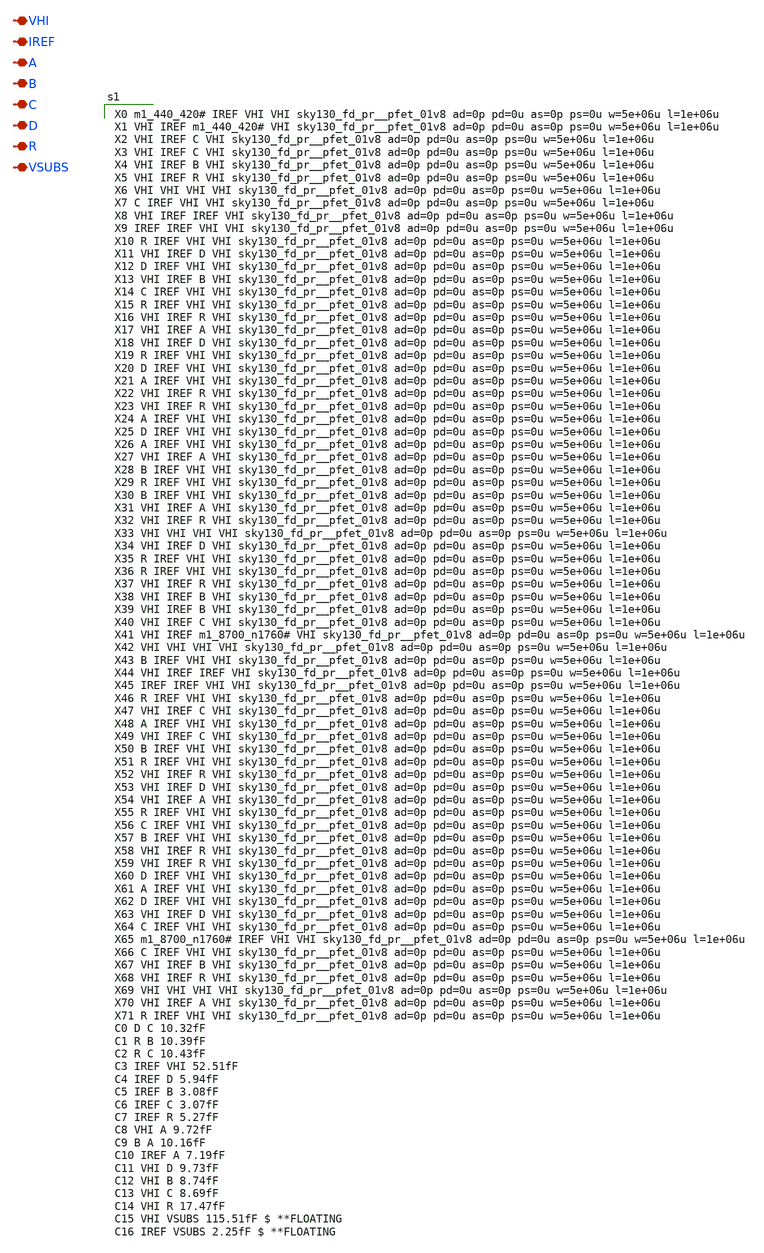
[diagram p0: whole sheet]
** sch_path: xschem/MIXER_current_dist_PEX.sch
**.subckt MIXER_current_dist_PEX IREF A B C D R VSUBS VHI
*.iopin IREF
*.iopin A
*.iopin B
*.iopin C
*.iopin D
*.iopin R
*.iopin VSUBS
*.iopin VHI
**** begin user architecture code

X0 m1_440_420# IREF VHI VHI sky130_fd_pr__pfet_01v8 ad=0p pd=0u as=0p ps=0u w=5e+06u l=1e+06u
X1 VHI IREF m1_440_420# VHI sky130_fd_pr__pfet_01v8 ad=0p pd=0u as=0p ps=0u w=5e+06u l=1e+06u
X2 VHI IREF C VHI sky130_fd_pr__pfet_01v8 ad=0p pd=0u as=0p ps=0u w=5e+06u l=1e+06u
X3 VHI IREF C VHI sky130_fd_pr__pfet_01v8 ad=0p pd=0u as=0p ps=0u w=5e+06u l=1e+06u
X4 VHI IREF B VHI sky130_fd_pr__pfet_01v8 ad=0p pd=0u as=0p ps=0u w=5e+06u l=1e+06u
X5 VHI IREF R VHI sky130_fd_pr__pfet_01v8 ad=0p pd=0u as=0p ps=0u w=5e+06u l=1e+06u
X6 VHI VHI VHI VHI sky130_fd_pr__pfet_01v8 ad=0p pd=0u as=0p ps=0u w=5e+06u l=1e+06u
X7 C IREF VHI VHI sky130_fd_pr__pfet_01v8 ad=0p pd=0u as=0p ps=0u w=5e+06u l=1e+06u
X8 VHI IREF IREF VHI sky130_fd_pr__pfet_01v8 ad=0p pd=0u as=0p ps=0u w=5e+06u l=1e+06u
X9 IREF IREF VHI VHI sky130_fd_pr__pfet_01v8 ad=0p pd=0u as=0p ps=0u w=5e+06u l=1e+06u
X10 R IREF VHI VHI sky130_fd_pr__pfet_01v8 ad=0p pd=0u as=0p ps=0u w=5e+06u l=1e+06u
X11 VHI IREF D VHI sky130_fd_pr__pfet_01v8 ad=0p pd=0u as=0p ps=0u w=5e+06u l=1e+06u
X12 D IREF VHI VHI sky130_fd_pr__pfet_01v8 ad=0p pd=0u as=0p ps=0u w=5e+06u l=1e+06u
X13 VHI IREF B VHI sky130_fd_pr__pfet_01v8 ad=0p pd=0u as=0p ps=0u w=5e+06u l=1e+06u
X14 C IREF VHI VHI sky130_fd_pr__pfet_01v8 ad=0p pd=0u as=0p ps=0u w=5e+06u l=1e+06u
X15 R IREF VHI VHI sky130_fd_pr__pfet_01v8 ad=0p pd=0u as=0p ps=0u w=5e+06u l=1e+06u
X16 VHI IREF R VHI sky130_fd_pr__pfet_01v8 ad=0p pd=0u as=0p ps=0u w=5e+06u l=1e+06u
X17 VHI IREF A VHI sky130_fd_pr__pfet_01v8 ad=0p pd=0u as=0p ps=0u w=5e+06u l=1e+06u
X18 VHI IREF D VHI sky130_fd_pr__pfet_01v8 ad=0p pd=0u as=0p ps=0u w=5e+06u l=1e+06u
X19 R IREF VHI VHI sky130_fd_pr__pfet_01v8 ad=0p pd=0u as=0p ps=0u w=5e+06u l=1e+06u
X20 D IREF VHI VHI sky130_fd_pr__pfet_01v8 ad=0p pd=0u as=0p ps=0u w=5e+06u l=1e+06u
X21 A IREF VHI VHI sky130_fd_pr__pfet_01v8 ad=0p pd=0u as=0p ps=0u w=5e+06u l=1e+06u
X22 VHI IREF R VHI sky130_fd_pr__pfet_01v8 ad=0p pd=0u as=0p ps=0u w=5e+06u l=1e+06u
X23 VHI IREF R VHI sky130_fd_pr__pfet_01v8 ad=0p pd=0u as=0p ps=0u w=5e+06u l=1e+06u
X24 A IREF VHI VHI sky130_fd_pr__pfet_01v8 ad=0p pd=0u as=0p ps=0u w=5e+06u l=1e+06u
X25 D IREF VHI VHI sky130_fd_pr__pfet_01v8 ad=0p pd=0u as=0p ps=0u w=5e+06u l=1e+06u
X26 A IREF VHI VHI sky130_fd_pr__pfet_01v8 ad=0p pd=0u as=0p ps=0u w=5e+06u l=1e+06u
X27 VHI IREF A VHI sky130_fd_pr__pfet_01v8 ad=0p pd=0u as=0p ps=0u w=5e+06u l=1e+06u
X28 B IREF VHI VHI sky130_fd_pr__pfet_01v8 ad=0p pd=0u as=0p ps=0u w=5e+06u l=1e+06u
X29 R IREF VHI VHI sky130_fd_pr__pfet_01v8 ad=0p pd=0u as=0p ps=0u w=5e+06u l=1e+06u
X30 B IREF VHI VHI sky130_fd_pr__pfet_01v8 ad=0p pd=0u as=0p ps=0u w=5e+06u l=1e+06u
X31 VHI IREF A VHI sky130_fd_pr__pfet_01v8 ad=0p pd=0u as=0p ps=0u w=5e+06u l=1e+06u
X32 VHI IREF R VHI sky130_fd_pr__pfet_01v8 ad=0p pd=0u as=0p ps=0u w=5e+06u l=1e+06u
X33 VHI VHI VHI VHI sky130_fd_pr__pfet_01v8 ad=0p pd=0u as=0p ps=0u w=5e+06u l=1e+06u
X34 VHI IREF D VHI sky130_fd_pr__pfet_01v8 ad=0p pd=0u as=0p ps=0u w=5e+06u l=1e+06u
X35 R IREF VHI VHI sky130_fd_pr__pfet_01v8 ad=0p pd=0u as=0p ps=0u w=5e+06u l=1e+06u
X36 R IREF VHI VHI sky130_fd_pr__pfet_01v8 ad=0p pd=0u as=0p ps=0u w=5e+06u l=1e+06u
X37 VHI IREF R VHI sky130_fd_pr__pfet_01v8 ad=0p pd=0u as=0p ps=0u w=5e+06u l=1e+06u
X38 VHI IREF B VHI sky130_fd_pr__pfet_01v8 ad=0p pd=0u as=0p ps=0u w=5e+06u l=1e+06u
X39 VHI IREF B VHI sky130_fd_pr__pfet_01v8 ad=0p pd=0u as=0p ps=0u w=5e+06u l=1e+06u
X40 VHI IREF C VHI sky130_fd_pr__pfet_01v8 ad=0p pd=0u as=0p ps=0u w=5e+06u l=1e+06u
X41 VHI IREF m1_8700_n1760# VHI sky130_fd_pr__pfet_01v8 ad=0p pd=0u as=0p ps=0u w=5e+06u l=1e+06u
X42 VHI VHI VHI VHI sky130_fd_pr__pfet_01v8 ad=0p pd=0u as=0p ps=0u w=5e+06u l=1e+06u
X43 B IREF VHI VHI sky130_fd_pr__pfet_01v8 ad=0p pd=0u as=0p ps=0u w=5e+06u l=1e+06u
X44 VHI IREF IREF VHI sky130_fd_pr__pfet_01v8 ad=0p pd=0u as=0p ps=0u w=5e+06u l=1e+06u
X45 IREF IREF VHI VHI sky130_fd_pr__pfet_01v8 ad=0p pd=0u as=0p ps=0u w=5e+06u l=1e+06u
X46 R IREF VHI VHI sky130_fd_pr__pfet_01v8 ad=0p pd=0u as=0p ps=0u w=5e+06u l=1e+06u
X47 VHI IREF C VHI sky130_fd_pr__pfet_01v8 ad=0p pd=0u as=0p ps=0u w=5e+06u l=1e+06u
X48 A IREF VHI VHI sky130_fd_pr__pfet_01v8 ad=0p pd=0u as=0p ps=0u w=5e+06u l=1e+06u
X49 VHI IREF C VHI sky130_fd_pr__pfet_01v8 ad=0p pd=0u as=0p ps=0u w=5e+06u l=1e+06u
X50 B IREF VHI VHI sky130_fd_pr__pfet_01v8 ad=0p pd=0u as=0p ps=0u w=5e+06u l=1e+06u
X51 R IREF VHI VHI sky130_fd_pr__pfet_01v8 ad=0p pd=0u as=0p ps=0u w=5e+06u l=1e+06u
X52 VHI IREF R VHI sky130_fd_pr__pfet_01v8 ad=0p pd=0u as=0p ps=0u w=5e+06u l=1e+06u
X53 VHI IREF D VHI sky130_fd_pr__pfet_01v8 ad=0p pd=0u as=0p ps=0u w=5e+06u l=1e+06u
X54 VHI IREF A VHI sky130_fd_pr__pfet_01v8 ad=0p pd=0u as=0p ps=0u w=5e+06u l=1e+06u
X55 R IREF VHI VHI sky130_fd_pr__pfet_01v8 ad=0p pd=0u as=0p ps=0u w=5e+06u l=1e+06u
X56 C IREF VHI VHI sky130_fd_pr__pfet_01v8 ad=0p pd=0u as=0p ps=0u w=5e+06u l=1e+06u
X57 B IREF VHI VHI sky130_fd_pr__pfet_01v8 ad=0p pd=0u as=0p ps=0u w=5e+06u l=1e+06u
X58 VHI IREF R VHI sky130_fd_pr__pfet_01v8 ad=0p pd=0u as=0p ps=0u w=5e+06u l=1e+06u
X59 VHI IREF R VHI sky130_fd_pr__pfet_01v8 ad=0p pd=0u as=0p ps=0u w=5e+06u l=1e+06u
X60 D IREF VHI VHI sky130_fd_pr__pfet_01v8 ad=0p pd=0u as=0p ps=0u w=5e+06u l=1e+06u
X61 A IREF VHI VHI sky130_fd_pr__pfet_01v8 ad=0p pd=0u as=0p ps=0u w=5e+06u l=1e+06u
X62 D IREF VHI VHI sky130_fd_pr__pfet_01v8 ad=0p pd=0u as=0p ps=0u w=5e+06u l=1e+06u
X63 VHI IREF D VHI sky130_fd_pr__pfet_01v8 ad=0p pd=0u as=0p ps=0u w=5e+06u l=1e+06u
X64 C IREF VHI VHI sky130_fd_pr__pfet_01v8 ad=0p pd=0u as=0p ps=0u w=5e+06u l=1e+06u
X65 m1_8700_n1760# IREF VHI VHI sky130_fd_pr__pfet_01v8 ad=0p pd=0u as=0p ps=0u w=5e+06u l=1e+06u
X66 C IREF VHI VHI sky130_fd_pr__pfet_01v8 ad=0p pd=0u as=0p ps=0u w=5e+06u l=1e+06u
X67 VHI IREF B VHI sky130_fd_pr__pfet_01v8 ad=0p pd=0u as=0p ps=0u w=5e+06u l=1e+06u
X68 VHI IREF R VHI sky130_fd_pr__pfet_01v8 ad=0p pd=0u as=0p ps=0u w=5e+06u l=1e+06u
X69 VHI VHI VHI VHI sky130_fd_pr__pfet_01v8 ad=0p pd=0u as=0p ps=0u w=5e+06u l=1e+06u
X70 VHI IREF A VHI sky130_fd_pr__pfet_01v8 ad=0p pd=0u as=0p ps=0u w=5e+06u l=1e+06u
X71 R IREF VHI VHI sky130_fd_pr__pfet_01v8 ad=0p pd=0u as=0p ps=0u w=5e+06u l=1e+06u
C0 D C 10.32fF
C1 R B 10.39fF
C2 R C 10.43fF
C3 IREF VHI 52.51fF
C4 IREF D 5.94fF
C5 IREF B 3.08fF
C6 IREF C 3.07fF
C7 IREF R 5.27fF
C8 VHI A 9.72fF
C9 B A 10.16fF
C10 IREF A 7.19fF
C11 VHI D 9.73fF
C12 VHI B 8.74fF
C13 VHI C 8.69fF
C14 VHI R 17.47fF
C15 VHI VSUBS 115.51fF $ **FLOATING
C16 IREF VSUBS 2.25fF $ **FLOATING



**** end user architecture code
**.ends
.end
